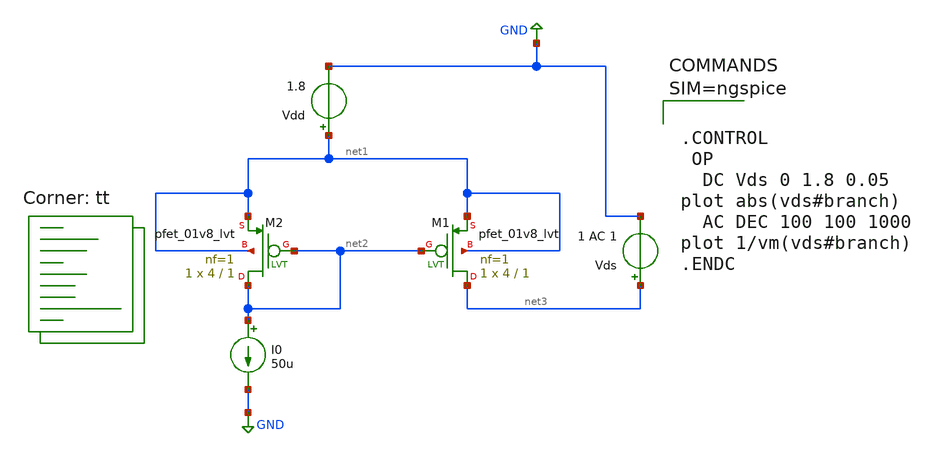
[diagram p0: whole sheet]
** sch_path: Work/xschem/currentmirror_2_pmos.sch
**.subckt currentmirror_2_pmos
XM1 net3 net2 net1 net1 sky130_fd_pr__pfet_01v8_lvt L=1 W=4 nf=1 ad='int((1 + 1)/2) * 4 / 1 * 0.29' as='int((1 + 2)/2) * 4 / 1 * 0.29'
+ pd='2*int((1 + 1)/2) * (4 / 1 + 0.29)' ps='2*int((1 + 2)/2) * (4 / 1 + 0.29)' nrd='0.29 / 4 ' nrs='0.29 / 4 '
+ sa=0 sb=0 sd=0 mult=1 m=1
XM2 net2 net2 net1 net1 sky130_fd_pr__pfet_01v8_lvt L=1 W=4 nf=1 ad='int((1 + 1)/2) * 4 / 1 * 0.29' as='int((1 + 2)/2) * 4 / 1 * 0.29'
+ pd='2*int((1 + 1)/2) * (4 / 1 + 0.29)' ps='2*int((1 + 2)/2) * (4 / 1 + 0.29)' nrd='0.29 / 4 ' nrs='0.29 / 4 '
+ sa=0 sb=0 sd=0 mult=1 m=1
I0 net2 GND 50u
Vds net3 GND 1 AC 1
Vdd net1 GND 1.8
**** begin user architecture code
.lib $::SKYWATER_MODELS/sky130.lib.spice tt



.CONTROL
 OP
  DC Vds 0 1.8 0.05
plot abs(vds#branch)
  AC DEC 100 100 1000
plot 1/vm(vds#branch)
.ENDC



.lib /usr/local/share/pdk/sky130A/libs.tech/ngspice/sky130.lib.spice tt
**** end user architecture code
**.ends
.GLOBAL GND
.end
